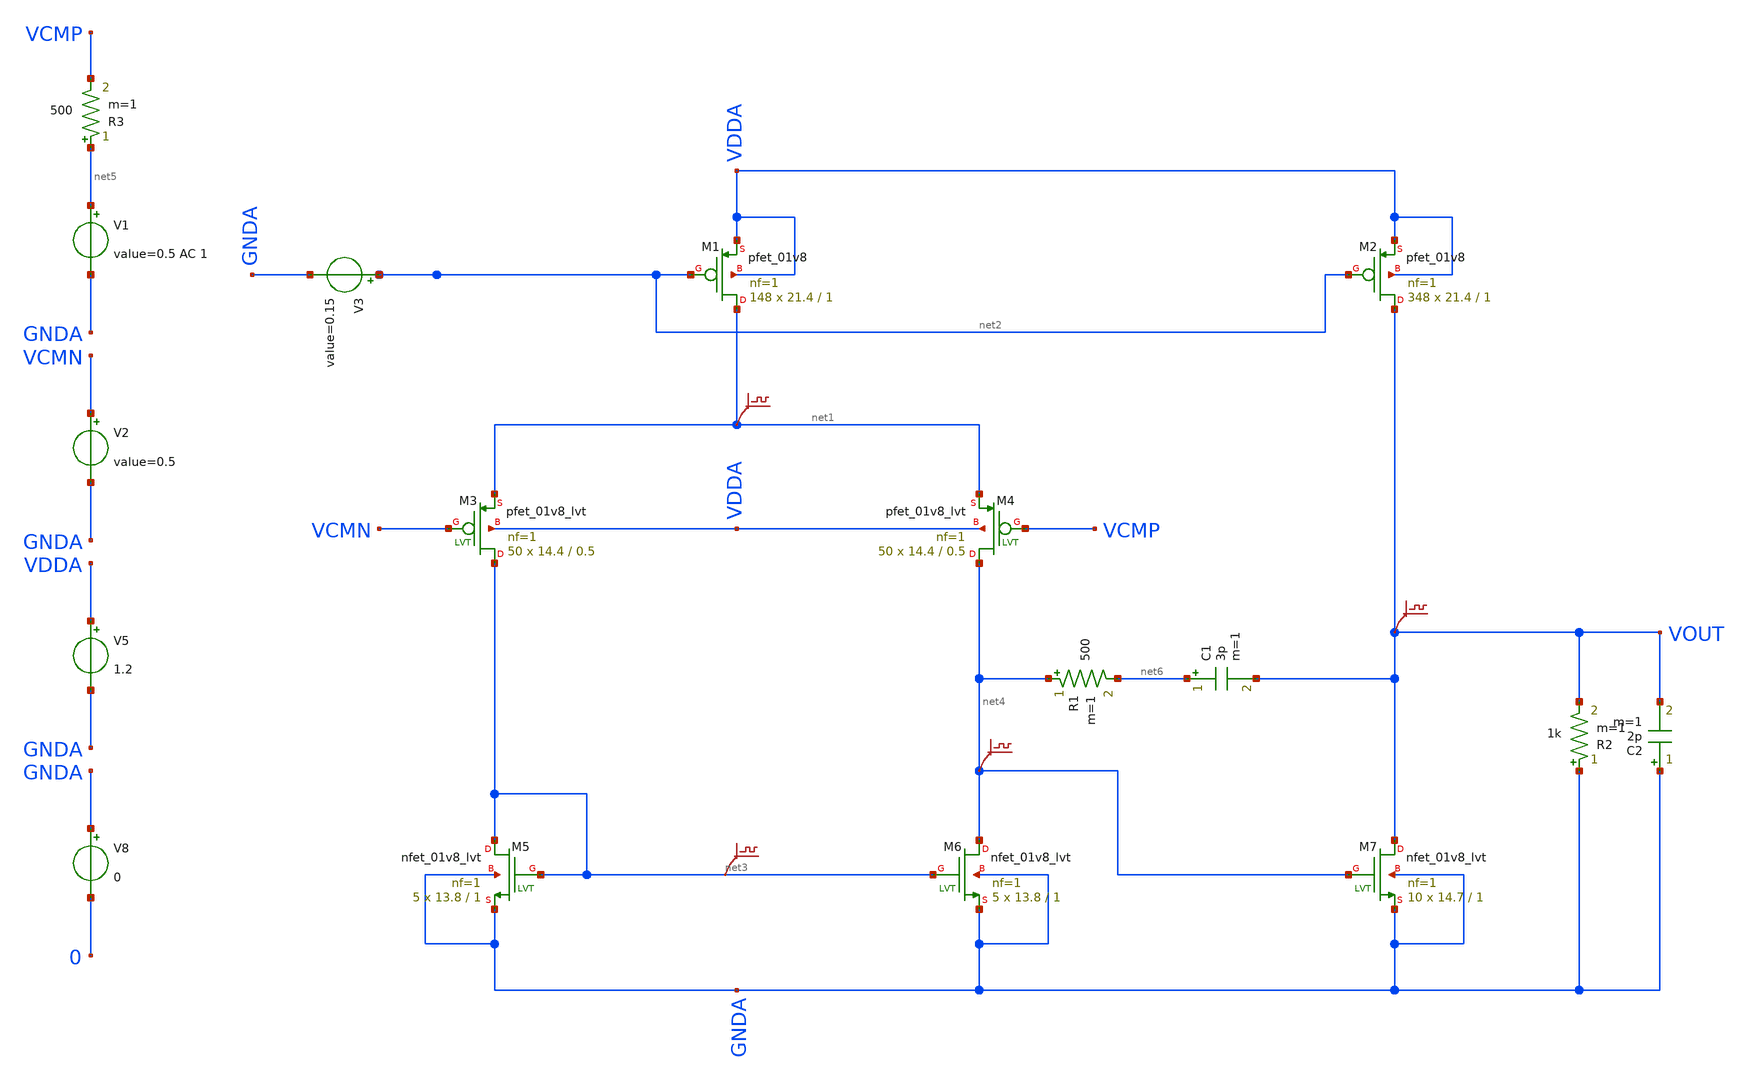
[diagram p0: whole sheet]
** sch_path: P_miller_ota.sch
**.subckt P_miller_ota
XM1 net1 net2 VDDA VDDA sky130_fd_pr__pfet_01v8 L=1 W=21.4 nf=1 ad='int((nf+1)/2) * W/nf * 0.29' as='int((nf+2)/2) * W/nf * 0.29'
+ pd='2*int((nf+1)/2) * (W/nf + 0.29)' ps='2*int((nf+2)/2) * (W/nf + 0.29)' nrd='0.29 / W' nrs='0.29 / W'
+ sa=0 sb=0 sd=0 mult=148 m=148
XM2 VOUT net2 VDDA VDDA sky130_fd_pr__pfet_01v8 L=1 W=21.4 nf=1 ad='int((nf+1)/2) * W/nf * 0.29' as='int((nf+2)/2) * W/nf * 0.29'
+ pd='2*int((nf+1)/2) * (W/nf + 0.29)' ps='2*int((nf+2)/2) * (W/nf + 0.29)' nrd='0.29 / W' nrs='0.29 / W'
+ sa=0 sb=0 sd=0 mult=348 m=348
XM3 net3 VCMN net1 VDDA sky130_fd_pr__pfet_01v8_lvt L=0.5 W=14.4 nf=1 ad='int((nf+1)/2) * W/nf * 0.29'
+ as='int((nf+2)/2) * W/nf * 0.29' pd='2*int((nf+1)/2) * (W/nf + 0.29)' ps='2*int((nf+2)/2) * (W/nf + 0.29)'
+ nrd='0.29 / W' nrs='0.29 / W' sa=0 sb=0 sd=0 mult=50 m=50
XM4 net4 VCMP net1 VDDA sky130_fd_pr__pfet_01v8_lvt L=0.5 W=14.4 nf=1 ad='int((nf+1)/2) * W/nf * 0.29'
+ as='int((nf+2)/2) * W/nf * 0.29' pd='2*int((nf+1)/2) * (W/nf + 0.29)' ps='2*int((nf+2)/2) * (W/nf + 0.29)'
+ nrd='0.29 / W' nrs='0.29 / W' sa=0 sb=0 sd=0 mult=50 m=50
XM5 net3 net3 GNDA GNDA sky130_fd_pr__nfet_01v8_lvt L=1 W=13.8 nf=1 ad='int((nf+1)/2) * W/nf * 0.29'
+ as='int((nf+2)/2) * W/nf * 0.29' pd='2*int((nf+1)/2) * (W/nf + 0.29)' ps='2*int((nf+2)/2) * (W/nf + 0.29)'
+ nrd='0.29 / W' nrs='0.29 / W' sa=0 sb=0 sd=0 mult=5 m=5
XM6 net4 net3 GNDA GNDA sky130_fd_pr__nfet_01v8_lvt L=1 W=13.8 nf=1 ad='int((nf+1)/2) * W/nf * 0.29'
+ as='int((nf+2)/2) * W/nf * 0.29' pd='2*int((nf+1)/2) * (W/nf + 0.29)' ps='2*int((nf+2)/2) * (W/nf + 0.29)'
+ nrd='0.29 / W' nrs='0.29 / W' sa=0 sb=0 sd=0 mult=5 m=5
XM7 VOUT net4 GNDA GNDA sky130_fd_pr__nfet_01v8_lvt L=1 W=14.7 nf=1 ad='int((nf+1)/2) * W/nf * 0.29'
+ as='int((nf+2)/2) * W/nf * 0.29' pd='2*int((nf+1)/2) * (W/nf + 0.29)' ps='2*int((nf+2)/2) * (W/nf + 0.29)'
+ nrd='0.29 / W' nrs='0.29 / W' sa=0 sb=0 sd=0 mult=10 m=10
R2 GNDA VOUT 1k m=1
C2 GNDA VOUT 2p m=1
V5 VDDA GNDA 1.2
V8 GNDA 0 0
V1 net5 GNDA 0.5 AC 1
V2 VCMN GNDA 0.5
R3 net5 VCMP 500 m=1
V3 net2 GNDA 0.15
.save v(net3)
.save v(vout)
.save v(net1)
.save v(net4)
R1 net4 net6 500 m=1
C1 net6 VOUT 3p m=1
**** begin user architecture code

** opencircuitdesign pdks install
.lib $::SKYWATER_MODELS/sky130.lib.spice tt




.control
save @m.xm1.msky130_fd_pr__pfet_01v8[vth]
save @m.xm1.msky130_fd_pr__pfet_01v8[id]
save @m.xm1.msky130_fd_pr__pfet_01v8[gds]
save @m.xm1.msky130_fd_pr__pfet_01v8[gm]
save @m.xm1.msky130_fd_pr__pfet_01v8[vdsat]
save @m.xm1.msky130_fd_pr__pfet_01v8[cgg]
save @m.xm1.msky130_fd_pr__pfet_01v8[cgd]

save @m.xm2.msky130_fd_pr__pfet_01v8[vth]
save @m.xm2.msky130_fd_pr__pfet_01v8[id]
save @m.xm2.msky130_fd_pr__pfet_01v8[gds]
save @m.xm2.msky130_fd_pr__pfet_01v8[gm]
save @m.xm2.msky130_fd_pr__pfet_01v8[vdsat]
save @m.xm2.msky130_fd_pr__pfet_01v8[cgg]
save @m.xm2.msky130_fd_pr__pfet_01v8[cgd]

save @m.xm3.msky130_fd_pr__pfet_01v8_lvt[vth]
save @m.xm3.msky130_fd_pr__pfet_01v8_lvt[id]
save @m.xm3.msky130_fd_pr__pfet_01v8_lvt[gds]
save @m.xm3.msky130_fd_pr__pfet_01v8_lvt[gm]
save @m.xm3.msky130_fd_pr__pfet_01v8_lvt[vdsat]
save @m.xm3.msky130_fd_pr__pfet_01v8_lvt[cgg]
save @m.xm3.msky130_fd_pr__pfet_01v8_lvt[cgd]

save @m.xm4.msky130_fd_pr__pfet_01v8_lvt[vth]
save @m.xm4.msky130_fd_pr__pfet_01v8_lvt[id]
save @m.xm4.msky130_fd_pr__pfet_01v8_lvt[gds]
save @m.xm4.msky130_fd_pr__pfet_01v8_lvt[gm]
save @m.xm4.msky130_fd_pr__pfet_01v8_lvt[vdsat]
save @m.xm4.msky130_fd_pr__pfet_01v8_lvt[cgg]
save @m.xm4.msky130_fd_pr__pfet_01v8_lvt[cgd]

save @m.xm5.msky130_fd_pr__nfet_01v8_lvt[vth]
save @m.xm5.msky130_fd_pr__nfet_01v8_lvt[id]
save @m.xm5.msky130_fd_pr__nfet_01v8_lvt[gds]
save @m.xm5.msky130_fd_pr__nfet_01v8_lvt[gm]
save @m.xm5.msky130_fd_pr__nfet_01v8_lvt[vdsat]
save @m.xm5.msky130_fd_pr__nfet_01v8_lvt[cgg]
save @m.xm5.msky130_fd_pr__nfet_01v8_lvt[cgd]

save @m.xm6.msky130_fd_pr__nfet_01v8_lvt[vth]
save @m.xm6.msky130_fd_pr__nfet_01v8_lvt[id]
save @m.xm6.msky130_fd_pr__nfet_01v8_lvt[gds]
save @m.xm6.msky130_fd_pr__nfet_01v8_lvt[gm]
save @m.xm6.msky130_fd_pr__nfet_01v8_lvt[vdsat]
save @m.xm6.msky130_fd_pr__nfet_01v8_lvt[cgg]
save @m.xm6.msky130_fd_pr__nfet_01v8_lvt[cgd]

save @m.xm7.msky130_fd_pr__nfet_01v8_lvt[vth]
save @m.xm7.msky130_fd_pr__nfet_01v8_lvt[id]
save @m.xm7.msky130_fd_pr__nfet_01v8_lvt[gds]
save @m.xm7.msky130_fd_pr__nfet_01v8_lvt[gm]
save @m.xm7.msky130_fd_pr__nfet_01v8_lvt[vdsat]
save @m.xm7.msky130_fd_pr__nfet_01v8_lvt[cgg]
save @m.xm7.msky130_fd_pr__nfet_01v8_lvt[cgd]

save all
op
ac dec 100 1 100T
*dc V1 0 1.2 0.0001
write P_miller_ota.raw

.endc


**** end user architecture code
**.ends
.end
